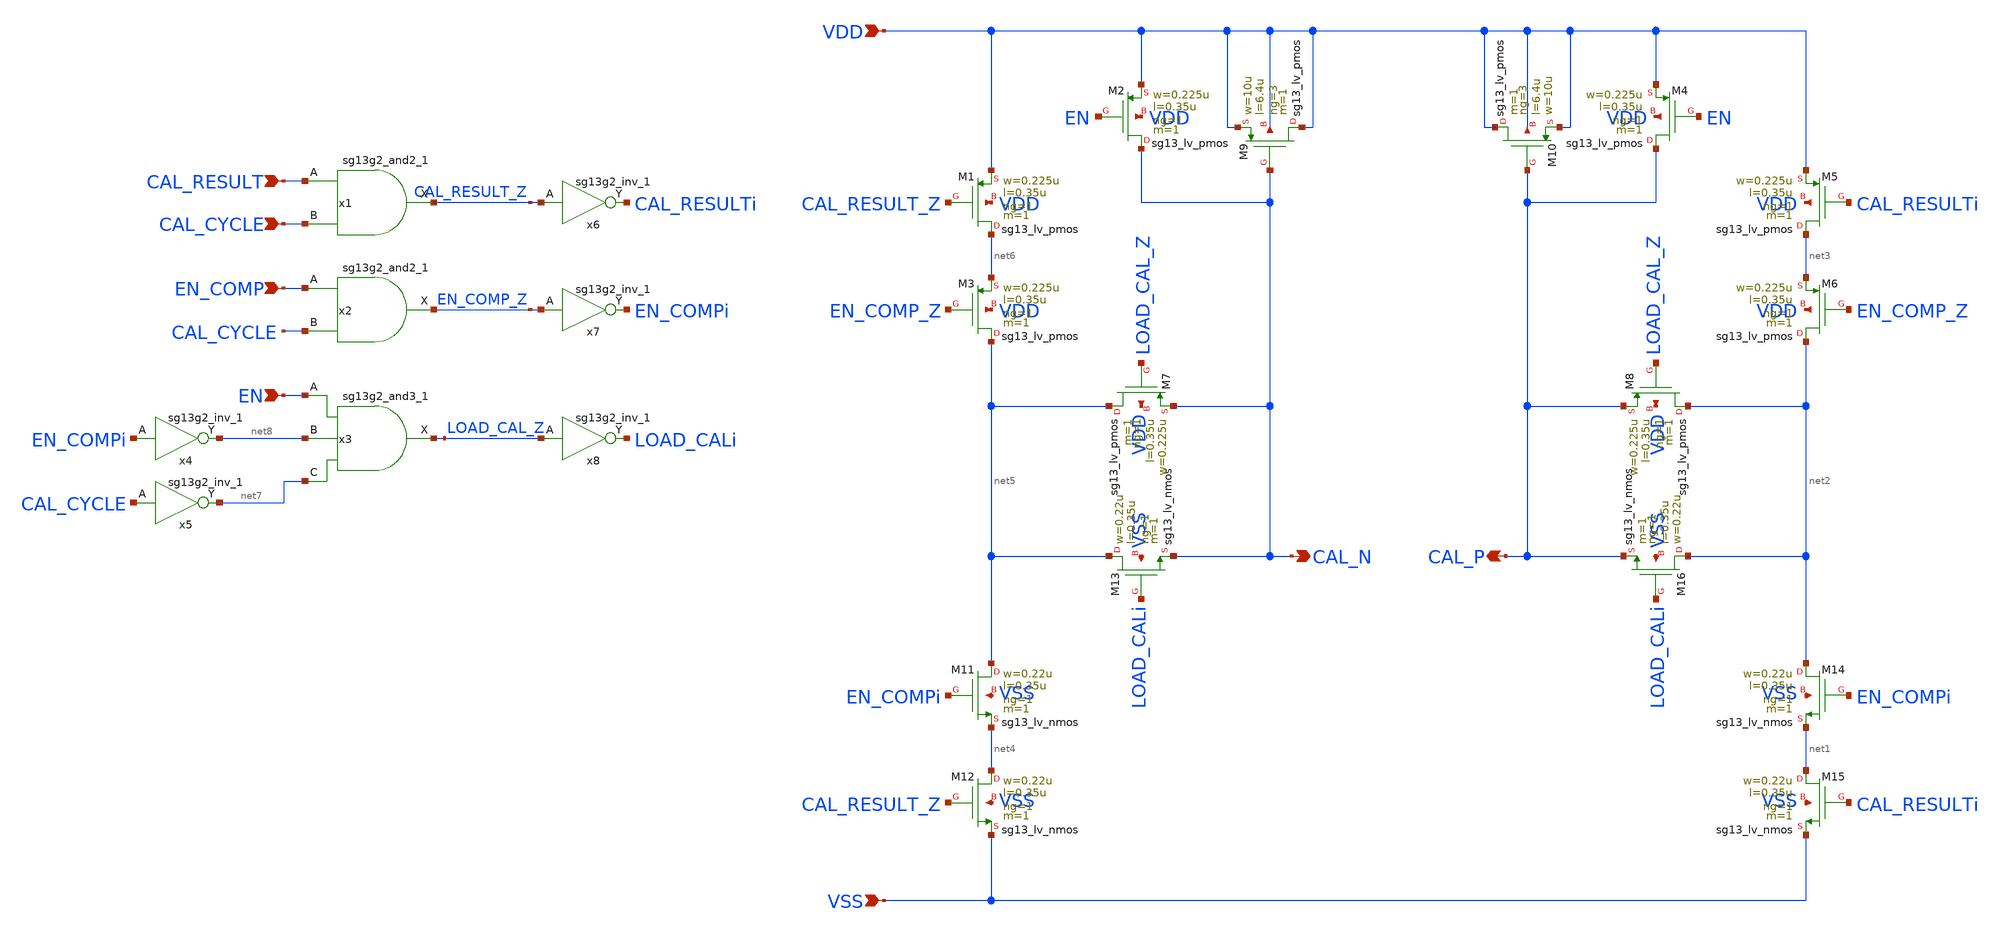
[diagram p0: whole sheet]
** sch_path: schematic/offset_calibration/offset_calibration-1.sch
* IHP-GmbH/IHP-Open-PDK/ihp-sg13g2/libs.tech/xschem/sg13g2_stdcells/sg13g2_and3_1.sch:
* Copyright 2023 IHP PDK Authors
* Licensed under the Apache License, Version 2.0 (the "License");
**.subckt offset_calibration-1 EN_COMP CAL_N CAL_P VDD VSS EN CAL_RESULT CAL_CYCLE
*.ipin EN_COMP
*.opin CAL_N
*.opin CAL_P
*.ipin VDD
*.ipin VSS
*.ipin EN
*.ipin CAL_RESULT
*.ipin CAL_CYCLE
XM2 CAL_N EN VDD VDD sg13_lv_pmos w=0.225u l=0.35u ng=1 m=1 mm_ok=1
XM1 net6 CAL_RESULT_Z VDD VDD sg13_lv_pmos w=0.225u l=0.35u ng=1 m=1 mm_ok=1
XM3 net5 EN_COMP_Z net6 VDD sg13_lv_pmos w=0.225u l=0.35u ng=1 m=1 mm_ok=1
XM4 CAL_P EN VDD VDD sg13_lv_pmos w=0.225u l=0.35u ng=1 m=1 mm_ok=1
XM5 net3 CAL_RESULTi VDD VDD sg13_lv_pmos w=0.225u l=0.35u ng=1 m=1 mm_ok=1
XM6 net2 EN_COMP_Z net3 VDD sg13_lv_pmos w=0.225u l=0.35u ng=1 m=1 mm_ok=1
XM7 net5 LOAD_CAL_Z CAL_N VDD sg13_lv_pmos w=0.225u l=0.35u ng=1 m=1 mm_ok=1
XM8 net2 LOAD_CAL_Z CAL_P VDD sg13_lv_pmos w=0.225u l=0.35u ng=1 m=1 mm_ok=1
XM9 VDD CAL_N VDD VDD sg13_lv_pmos w=10u l=6.4u ng=3 m=1 mm_ok=1
XM10 VDD CAL_P VDD VDD sg13_lv_pmos w=10u l=6.4u ng=3 m=1 mm_ok=1
XM11 net5 EN_COMPi net4 VSS sg13_lv_nmos w=0.22u l=0.35u ng=1 m=1 mm_ok=1
XM12 net4 CAL_RESULT_Z VSS VSS sg13_lv_nmos w=0.22u l=0.35u ng=1 m=1 mm_ok=1
XM13 net5 LOAD_CALi CAL_N VSS sg13_lv_nmos w=0.22u l=0.35u ng=1 m=1 mm_ok=1
XM14 net2 EN_COMPi net1 VSS sg13_lv_nmos w=0.22u l=0.35u ng=1 m=1 mm_ok=1
XM15 net1 CAL_RESULTi VSS VSS sg13_lv_nmos w=0.22u l=0.35u ng=1 m=1 mm_ok=1
XM16 net2 LOAD_CALi CAL_P VSS sg13_lv_nmos w=0.22u l=0.35u ng=1 m=1 mm_ok=1
x1 CAL_RESULT_Z CAL_RESULT CAL_CYCLE VDD VSS sg13g2_and2_1
x2 EN_COMP_Z EN_COMP CAL_CYCLE VDD VSS sg13g2_and2_1
x3 LOAD_CAL_Z EN net8 net7 VDD VSS sg13g2_and3_1
x4 net8 EN_COMPi VDD VSS sg13g2_inv_1
x5 net7 CAL_CYCLE VDD VSS sg13g2_inv_1
x6 CAL_RESULTi CAL_RESULT_Z VDD VSS sg13g2_inv_1
x7 EN_COMPi EN_COMP_Z VDD VSS sg13g2_inv_1
x8 LOAD_CALi LOAD_CAL_Z VDD VSS sg13g2_inv_1
**.ends

* expanding   symbol:  sg13g2_stdcells/sg13g2_and2_1.sym # of pins=3
** sym_path: sg13g2_stdcells/sg13g2_and2_1.sym
** sch_path: sg13g2_stdcells/sg13g2_and2_1.sch
.subckt sg13g2_and2_1 X A B VDD VSS
*.ipin A
*.ipin B
*.opin X
*.iopin VDD
*.iopin VSS
XM1 net1 A net2 VSS sg13_lv_nmos w=640.00n l=130.00n ng=1 m=1 mm_ok=1
XM2 net2 B VSS VSS sg13_lv_nmos w=640.00n l=130.00n ng=1 m=1 mm_ok=1
XM3 X net1 VSS VSS sg13_lv_nmos w=740.00n l=130.00n ng=1 m=1 mm_ok=1
XM4 net1 B VDD VDD sg13_lv_pmos w=840.00n l=130.00n ng=1 m=1 mm_ok=1
XM5 net1 A VDD VDD sg13_lv_pmos w=840.00n l=130.00n ng=1 m=1 mm_ok=1
XM6 X net1 VDD VDD sg13_lv_pmos w=1.12u l=130.00n ng=1 m=1 mm_ok=1
.ends


* expanding   symbol:  sg13g2_stdcells/sg13g2_and3_1.sym # of pins=4
** sym_path: sg13g2_stdcells/sg13g2_and3_1.sym
** sch_path: sg13g2_stdcells/sg13g2_and3_1.sch
.subckt sg13g2_and3_1 X A B C VDD VSS
*.opin X
*.ipin C
*.ipin B
*.ipin A
*.iopin VDD
*.iopin VSS
XM1 net2 A net3 VSS sg13_lv_nmos w=640.00n l=130.00n ng=1 m=1 mm_ok=1
XM2 net3 B net1 VSS sg13_lv_nmos w=640.00n l=130.00n ng=1 m=1 mm_ok=1
XM3 net1 C VSS VSS sg13_lv_nmos w=640.00n l=130.00n ng=1 m=1 mm_ok=1
XM4 X net2 VSS VSS sg13_lv_nmos w=740.00n l=130.00n ng=1 m=1 mm_ok=1
XM5 net2 C VDD VDD sg13_lv_pmos w=840.00n l=130.00n ng=1 m=1 mm_ok=1
XM6 net2 B VDD VDD sg13_lv_pmos w=840.00n l=130.00n ng=1 m=1 mm_ok=1
XM7 net2 A VDD VDD sg13_lv_pmos w=840.00n l=130.00n ng=1 m=1 mm_ok=1
XM8 X net2 VDD VDD sg13_lv_pmos w=1.12u l=130.00n ng=1 m=1 mm_ok=1
.ends


* expanding   symbol:  sg13g2_stdcells/sg13g2_inv_1.sym # of pins=2
** sym_path: sg13g2_stdcells/sg13g2_inv_1.sym
** sch_path: sg13g2_stdcells/sg13g2_inv_1.sch
.subckt sg13g2_inv_1 Y A VDD VSS
*.opin Y
*.ipin A
*.iopin VDD
*.iopin VSS
XM1 Y A VSS VSS sg13_lv_nmos w=740.00n l=130.00n ng=1 m=1 mm_ok=1
XM2 Y A VDD VDD sg13_lv_pmos w=1.12u l=130.00n ng=1 m=1 mm_ok=1
.ends

.end
